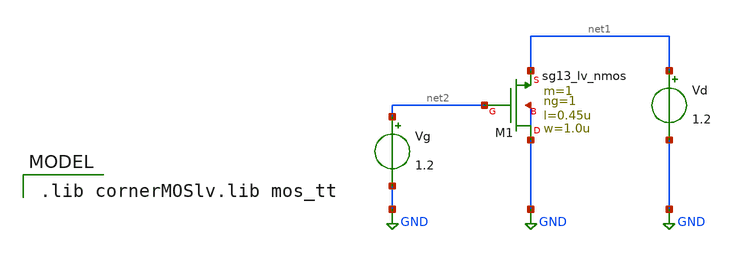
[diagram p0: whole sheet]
** sch_path: Taller1/Resuelto/NMoslv_test.sch
**.subckt NMoslv_test
XM1 GND net2 net1 GND sg13_lv_nmos w=1.0u l=0.45u ng=1 m=1 mm_ok=1
Vg net2 GND 1.2
Vd net1 GND 1.2
**** begin user architecture code
 .lib cornerMOSlv.lib mos_tt




.control
save all
save @n.xm1.nsg13_lv_nmos[gm]
save @n.xm1.nsg13_lv_nmos[ids]
dc vg 0.0 1.5 0.01
let id = @n.xm1.nsg13_lv_nmos[ids]
plot id
plot log(id)
.endc


**** end user architecture code
**.ends
.GLOBAL GND
.end
